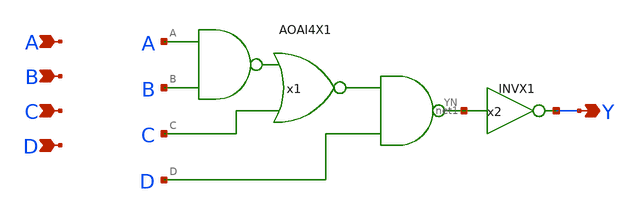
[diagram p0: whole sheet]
** sch_path: archives/lib/xschem/AOA4X1.sch
**.subckt AOA4X1 Y A B C D
*.opin Y
*.ipin A
*.ipin B
*.ipin C
*.ipin D
x1 net1 A B C D VDD VSS AOAI4X1
x2 Y net1 VDD VSS INVX1
**.ends
.end
